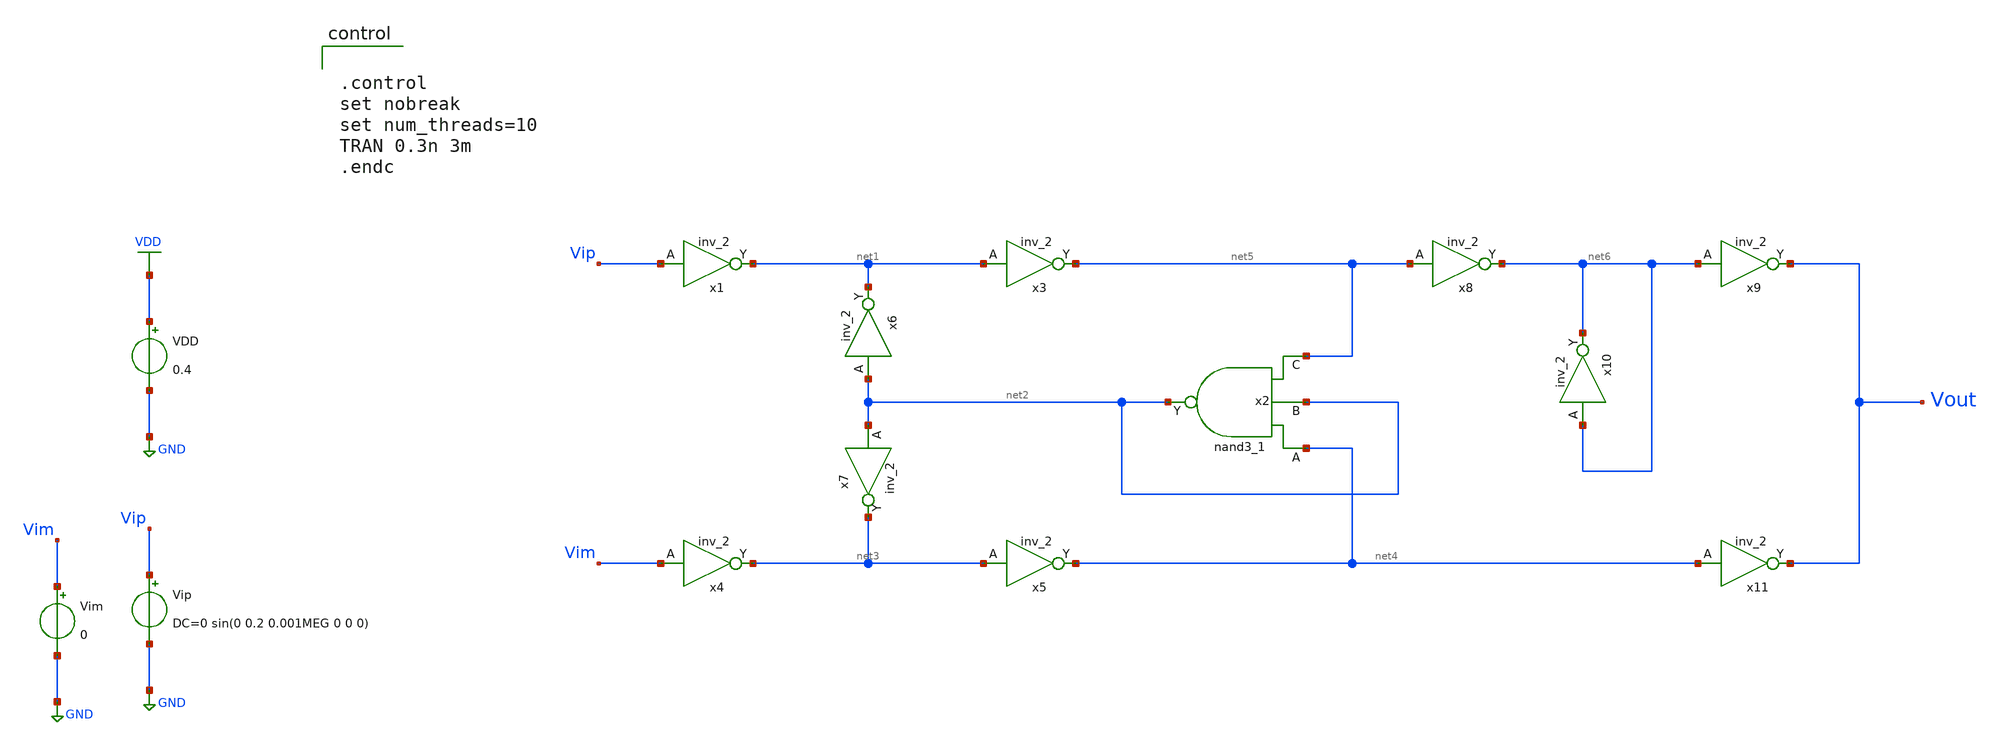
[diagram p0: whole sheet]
** sch_path: circuit_1.sch
**.subckt circuit_1
x1 Vip GND GND VDD VDD net1 sky130_fd_sc_hd__inv_2
x2 net4 net2 net5 GND GND VDD VDD net2 sky130_fd_sc_hd__nand3_1
x3 net1 GND GND VDD VDD net5 sky130_fd_sc_hd__inv_2
x4 Vim GND GND VDD VDD net3 sky130_fd_sc_hd__inv_2
x5 net3 GND GND VDD VDD net4 sky130_fd_sc_hd__inv_2
x6 net2 GND GND VDD VDD net1 sky130_fd_sc_hd__inv_2
x7 net2 GND GND VDD VDD net3 sky130_fd_sc_hd__inv_2
x8 net5 GND GND VDD VDD net6 sky130_fd_sc_hd__inv_2
x9 net6 GND GND VDD VDD Vout sky130_fd_sc_hd__inv_2
x10 net6 GND GND VDD VDD net6 sky130_fd_sc_hd__inv_2
x11 net4 GND GND VDD VDD Vout sky130_fd_sc_hd__inv_2
VDD VDD GND 0.4
Vip Vip GND DC=0 sin(0 0.2 0.001MEG 0 0 0)
Vim Vim GND 0
**** begin user architecture code


.control
set nobreak
set num_threads=10
TRAN 0.3n 3m
.endc




.inc /home/dkits/openpdks/sky130A/libs.ref/sky130_fd_sc_hd/spice/sky130_fd_sc_hd.spice
.lib /home/dkits/openpdks/sky130A/libs.tech/ngspice/sky130.lib.spice tt


**** end user architecture code
**.ends
.GLOBAL GND
.GLOBAL VDD
.end
